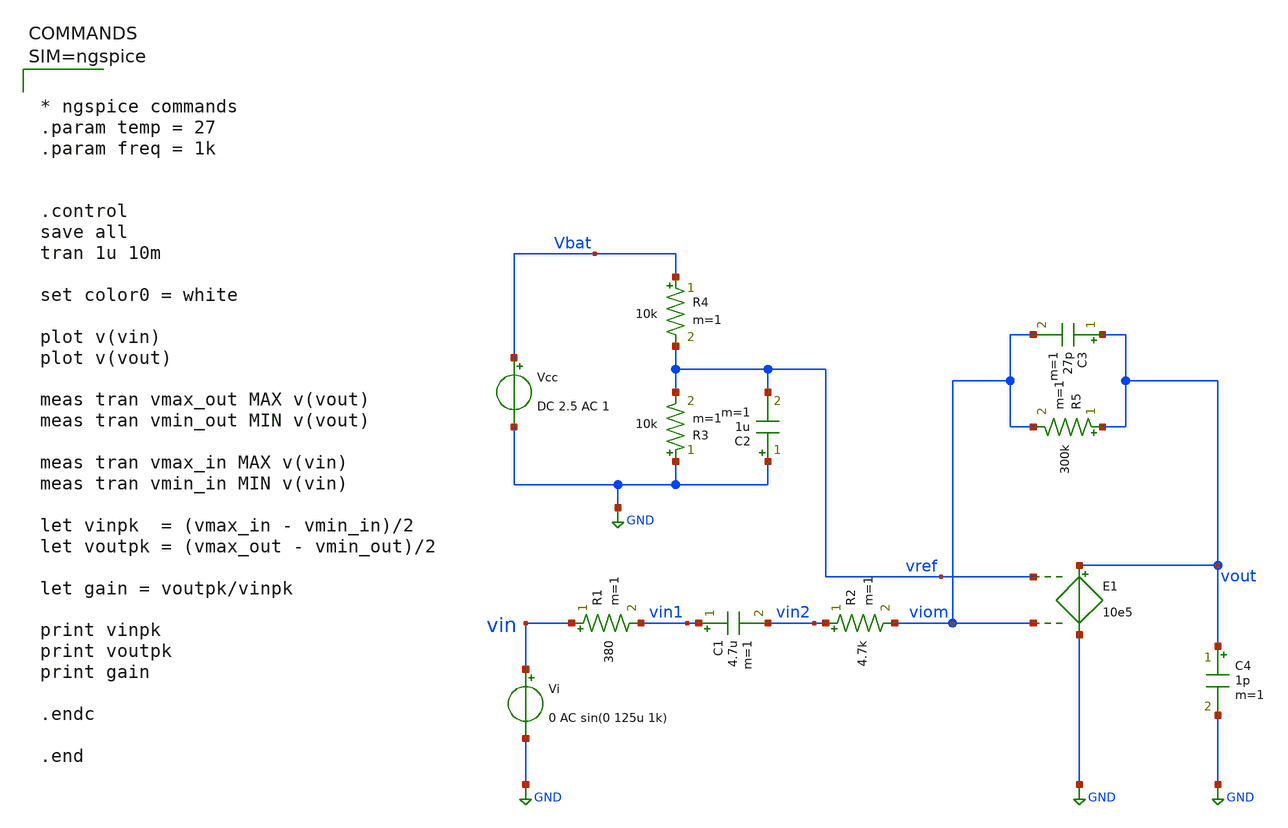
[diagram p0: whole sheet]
** sch_path: testbenches/MEMS_mic_transient_analysis.sch
**.subckt MEMS_mic_transient_analysis
R1 vin vin1 380 m=1
C1 vin1 vin2 4.7u m=1
R2 vin2 viom 4.7k m=1
E1 vout GND vref viom 10e5
Vi vin GND 0 AC sin(0 125u 1k)
R3 GND vref 10k m=1
C2 GND vref 1u m=1
R4 Vbat vref 10k m=1
Vcc Vbat GND DC 2.5 AC 1
R5 vout viom 300k m=1
C3 vout viom 27p m=1
C4 vout GND 1p m=1
**** begin user architecture code



* ngspice commands
.param temp = 27
.param freq = 1k


.control
save all
tran 1u 10m

set color0 = white

plot v(vin)
plot v(vout)

meas tran vmax_out MAX v(vout)
meas tran vmin_out MIN v(vout)

meas tran vmax_in MAX v(vin)
meas tran vmin_in MIN v(vin)

let vinpk  = (vmax_in - vmin_in)/2
let voutpk = (vmax_out - vmin_out)/2

let gain = voutpk/vinpk

print vinpk
print voutpk
print gain

.endc

.end



**** end user architecture code
**.ends
.GLOBAL GND
.end
